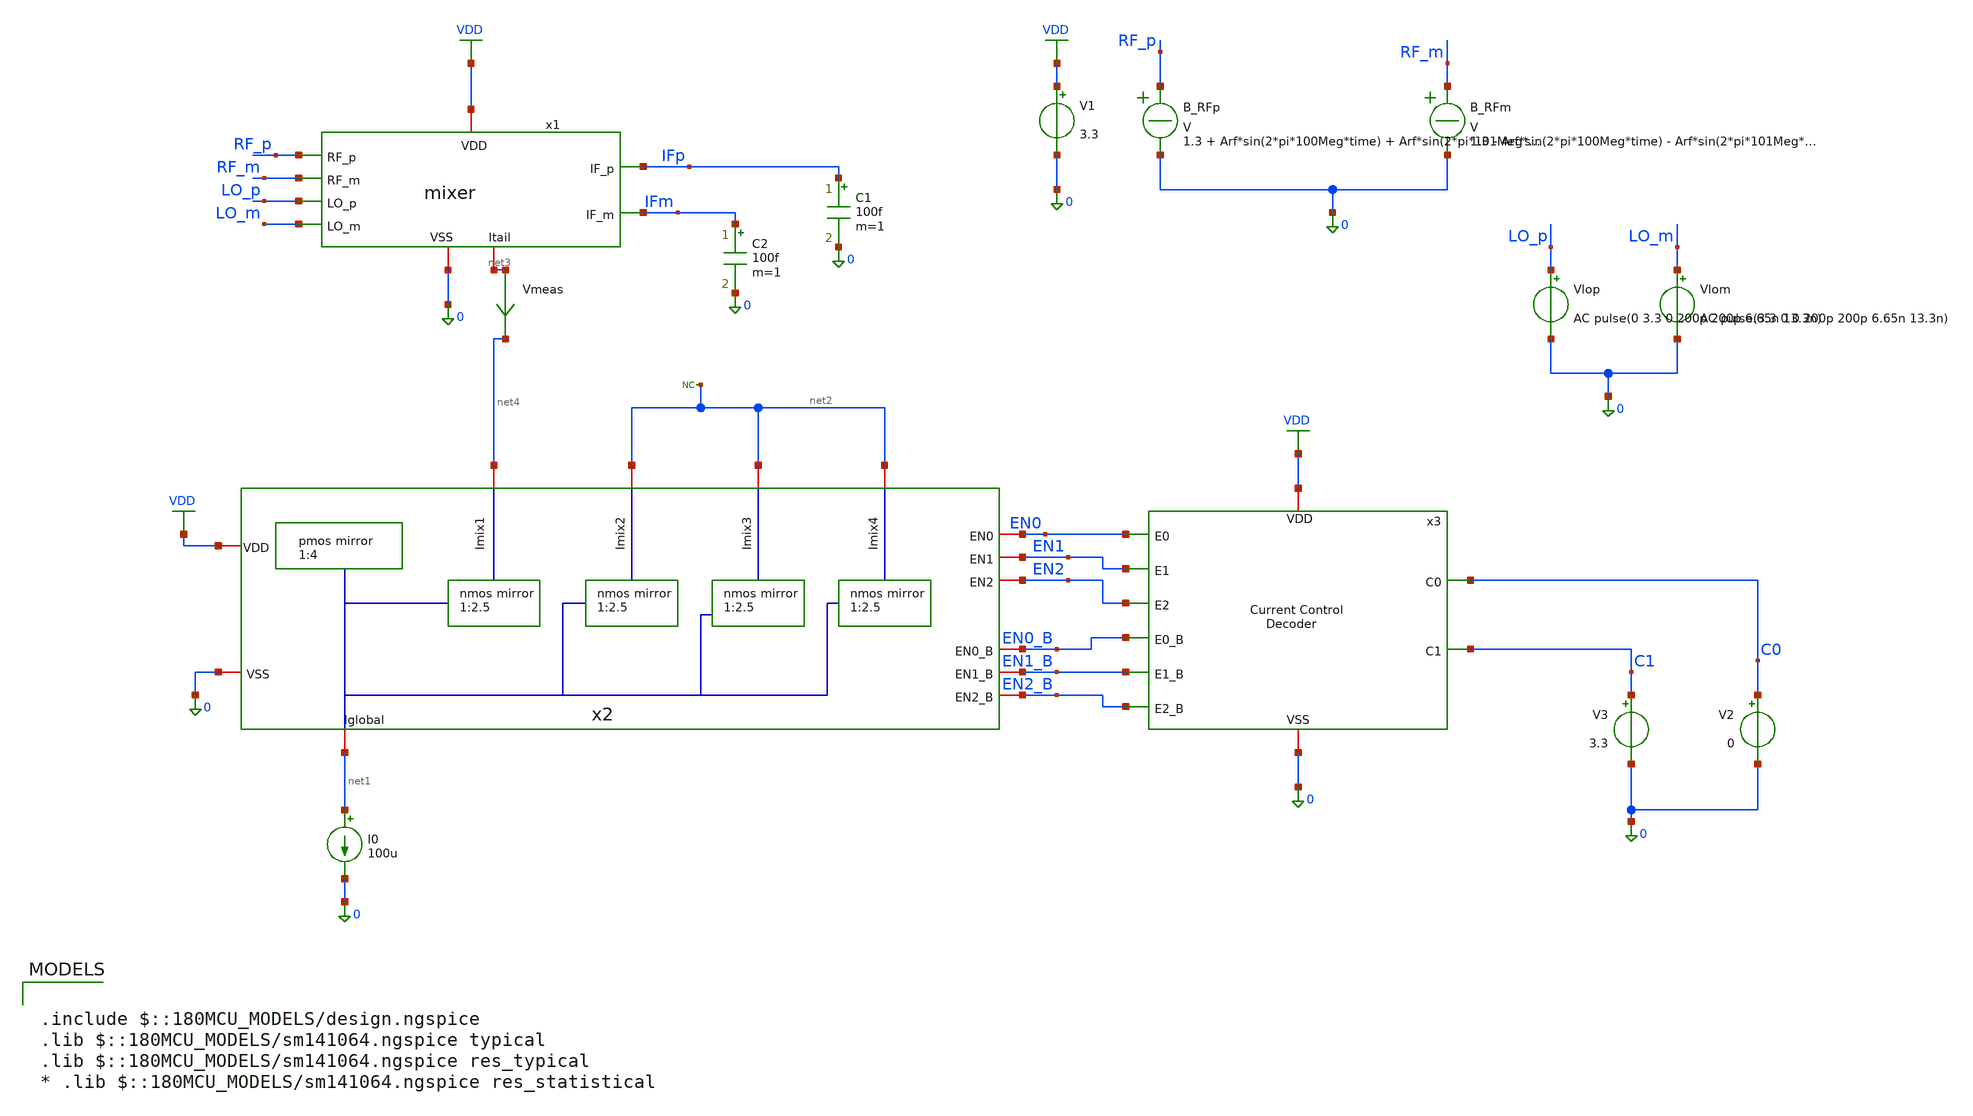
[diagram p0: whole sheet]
** sch_path: designs/mixer/testbench/mixer_iip3_tb.sch
**.subckt mixer_iip3_tb
V1 VDD 0 3.3
Vlop LO_p 0 AC pulse(0 3.3 0 200p 200p 6.65n 13.3n)
Vlom LO_m 0 AC pulse(3.3 0 0 200p 200p 6.65n 13.3n)
C1 IFp 0 100f m=1
C2 IFm 0 100f m=1
I0 net1 0 100u
* noconn #net2
x1 IFp RF_p VDD 0 IFm RF_m LO_p net3 LO_m mixer
Vmeas net3 net4 0
.save i(vmeas)
x2 EN2 EN1 EN0 EN0_B EN1_B EN2_B VDD net1 net2 net4 0 net2 net2 mirror_network_with_enable
V2 C0 0 0
V3 C1 0 3.3
x3 VDD C0 EN2 C1 0 EN1 EN0 EN2_B EN1_B EN0_B decoder
B_RFp RF_p 0 V = 1.3 + Arf*sin(2*pi*100Meg*time) + Arf*sin(2*pi*101Meg*time)
B_RFm RF_m 0 V = 1.3 - Arf*sin(2*pi*100Meg*time) - Arf*sin(2*pi*101Meg*time)
**** begin user architecture code

.include $::180MCU_MODELS/design.ngspice
.lib $::180MCU_MODELS/sm141064.ngspice typical
.lib $::180MCU_MODELS/sm141064.ngspice res_typical
* .lib $::180MCU_MODELS/sm141064.ngspice res_statistical



.param Arf=10m
.control

destroy all

op
echo Itail
print i(vmeas)

foreach A 3m 4m 175m
	alterparam Arf = $A
	reset
	save v(ifp) v(ifm)
	tran 0.05n 25u ;transient sim

	let vif = V(IFp)-V(IFm)

	fft vif
	plot db(mag(vif)) vs frequency xlimit 20Meg 30Meg
	plot mag(vif) vs frequency xlimit 20Meg 30Meg
end

.endc


**** end user architecture code
**.ends
.GLOBAL VDD
.end
